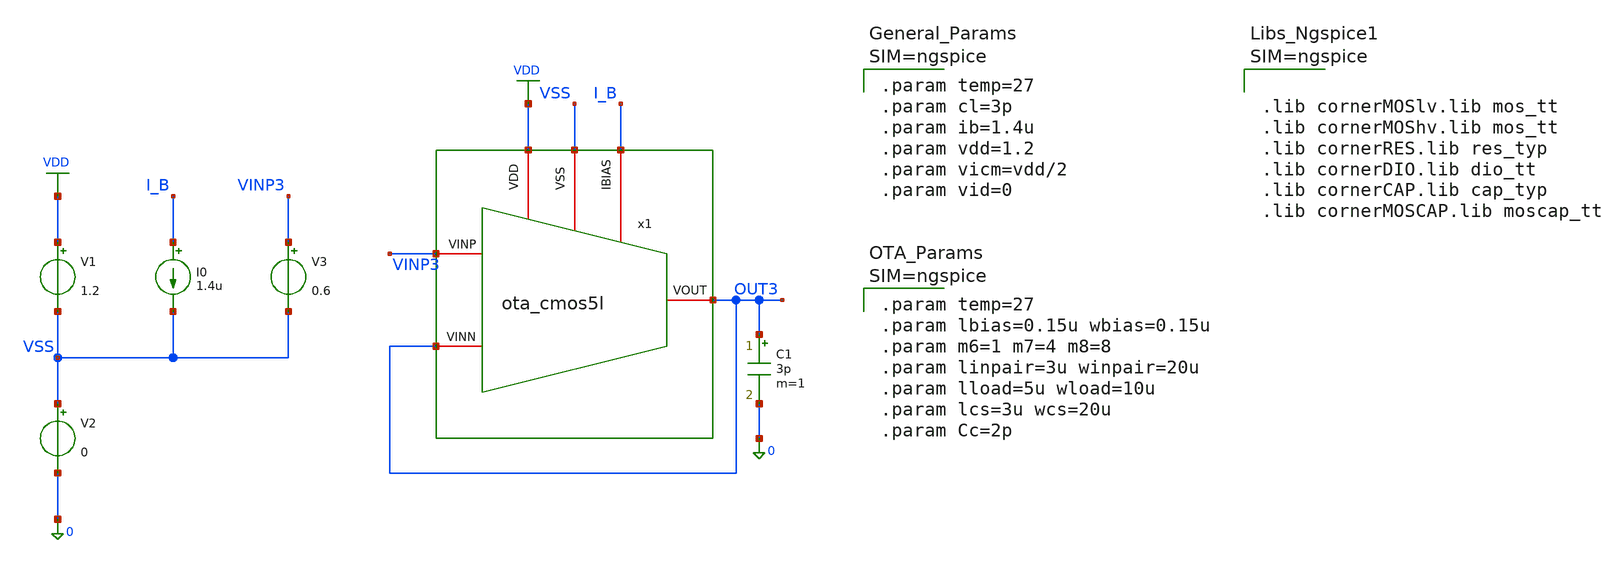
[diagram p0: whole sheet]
** sch_path: xschem/ota_cmos5l/tb/tb_ota_cmos5l_TRAN_small/tb_ota_cmos5l_TRAN_small.sch
**.subckt tb_ota_cmos5l_TRAN_small
x1 VSS I_B VDD OUT3 VINP3 OUT3 ota_cmos5l
C1 OUT3 0 3p m=1
I0 I_B VSS 1.4u
V1 VDD VSS 1.2
V2 VSS 0 0
V3 VINP3 VSS 0.6
**** begin user architecture code



.lib cornerMOSlv.lib mos_tt
.lib cornerMOShv.lib mos_tt
.lib cornerRES.lib res_typ
.lib cornerDIO.lib dio_tt
.lib cornerCAP.lib cap_typ
.lib cornerMOSCAP.lib moscap_tt





.param temp=27
.param cl=3p
.param ib=1.4u
.param vdd=1.2
.param vicm=vdd/2
.param vid=0





.param temp=27
.param lbias=0.15u wbias=0.15u
.param m6=1 m7=4 m8=8
.param linpair=3u winpair=20u
.param lload=5u wload=10u
.param lcs=3u wcs=20u
.param Cc=2p





.control
save all
shell mkdir -p result

* SMALL-SIGNAL STEP RESPONSE (SETTLING TIME & OVERSHOOT)
* Stimulus: Small step 0.55 V to 0.65 V (Delta V = 100 mV)
alter @v3[pulse] = [ 0.55 0.65 20n 1n 1n 500n 1.2u ]

tran 0.1n 1.2u
run

let v_ins  = v(vinp3)
let v_outs = v(out3)

* --- Small-Signal Delay and Rise Time ---
meas tran t_in_s50  when v_ins=0.60 rise=1
meas tran t_out_s10 when v_outs=0.56 rise=1
meas tran t_out_s50 when v_outs=0.60 rise=1
meas tran t_out_s90 when v_outs=0.64 rise=1

let t_delay_ns = (t_out_s50 - t_in_s50) * 1e9
let t_rise_ns  = (t_out_s90 - t_out_s10) * 1e9

* --- Overshoot Percentage ---
meas tran v_peak max v_outs from=20n to=300n
let overshoot_pct = ((v_peak - 0.65) / 0.1) * 100

* --- Settling Time Calculation ---
* Target value = 0.65 V (Step amplitude = 100 mV)
* 1% Band   : 0.65 V +/- 1 mV   -> 0.649 V to 0.651 V
* 0.1% Band : 0.65 V +/- 0.1 mV -> 0.6499 V to 0.6501 V
meas tran t_set1 when v_outs=0.649 cross=last
let ts_1pct_ns = (t_set1 - 20n) * 1e9

meas tran t_set01 when v_outs=0.6499 cross=last
let ts_01pct_ns = (t_set01 - 20n) * 1e9

* Save output waveforms to the specified rawfile
write ./result/tb_cg_ota_tran_small.raw v_ins v_outs

* Print execution summary
echo "======================================================="
echo "   OTA SMALL-SIGNAL TRANSIENT SIMULATION RESULTS       "
echo "======================================================="
echo " Small-Signal Delay        : " $&t_delay_ns   " ns"
echo " Small-Signal Rise Time    : " $&t_rise_ns    " ns"
echo " Peak Voltage (Vpeak)      : " $&v_peak       " V"
echo " Overshoot                 : " $&overshoot_pct " % (Target: < 10%)"
echo " Settling Time (1% Band)   : " $&ts_1pct_ns   " ns"
echo " Settling Time (0.1% Band) : " $&ts_01pct_ns  " ns"
echo "======================================================="

* Reset v5 source back to clean DC operating point
alter @v5[pulse] = [ 0.6 0.6 0 0 0 1u 2u ]

plot v_outs v_ins
.endc


**** end user architecture code
**.ends

* expanding   symbol:  /foss/designs/sg13cmos5l_spma_ip__instramp/xschem/ota_cmos5l/ota_cmos5l.sym #
*+ of pins=6
** sym_path: xschem/output_buffer/ota_cmos5l.sym
** sch_path: xschem/output_buffer/ota_cmos5l.sch
.subckt ota_cmos5l VSS IBIAS VDD VINN VINP VOUT
*.iopin IBIAS
*.iopin VDD
*.iopin VSS
*.iopin VOUT
*.iopin VINP
*.iopin VINN
XM6 IBIAS IBIAS VDD VDD sg13_lv_pmos w={wbias} l={lbias} ng=1 m={m6} mm_ok=1
XM7 net1 IBIAS VDD VDD sg13_lv_pmos w={wbias} l={lbias} ng=1 m={m7} mm_ok=1
XM8 VOUT IBIAS VDD VDD sg13_lv_pmos w={wbias} l={lbias} ng=1 m={m8} mm_ok=1
XM1 net2 VINN net1 VDD sg13_lv_pmos w={winpair} l={linpair} ng=1 m=1 mm_ok=1
XM2 net3 VINP net1 VDD sg13_lv_pmos w={winpair} l={linpair} ng=1 m=1 mm_ok=1
XM3 net2 net2 VSS VSS sg13_lv_nmos w={wload} l={lload} ng=1 m=1 mm_ok=1
XM4 net3 net2 VSS VSS sg13_lv_nmos w={wload} l={lload} ng=1 m=1 mm_ok=1
XM5 VOUT net3 VSS VSS sg13_lv_nmos w={wcs} l={lcs} ng=1 m=1 mm_ok=1
XR1 net3 net4 VSS rhigh w=0.5e-6 l=1.95e-6 m=1 b=0 mm_ok=1
.save v(vinp)
.save v(vinn)
.save v(vout)
XC2 VOUT net4 cap_cmomi w=15e-6 l=15e-6 mmin=1 mmax=4 feed=double subblock=0 m=5 mm_ok=1
**** begin user architecture code


.param temp=27
.param lbias=0.15u wbias=0.15u
.param m6=1 m7=4 m8=8
.param linpair=3u winpair=20u
.param lload=5u wload=10u
.param lcs=3u wcs=20u
.param Cc=2p



**** end user architecture code
XC1 VOUT net4 cap_cmomi w=15e-6 l=15e-6 mmin=1 mmax=4 feed=double subblock=0 m=4 mm_ok=1
.ends

.GLOBAL VDD
.end
